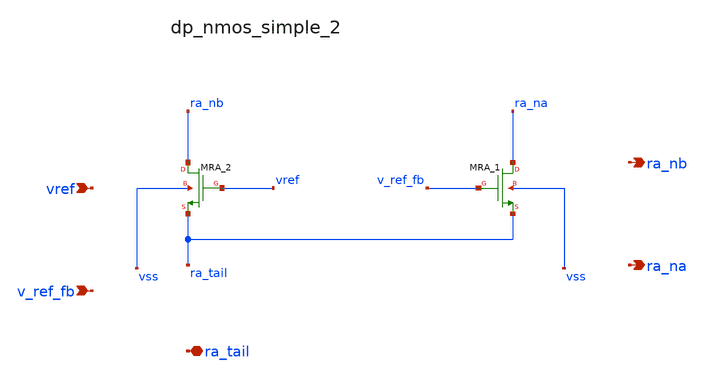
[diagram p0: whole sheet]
** sch_path: analog-db/raw/ldo_005_buffered_ref/hier/blocks/dp_nmos_simple_2.sch
**.subckt dp_nmos_simple_2 vref v_ref_fb ra_tail ra_nb ra_na
*.ipin vref
*.ipin v_ref_fb
*.iopin ra_tail
*.opin ra_nb
*.opin ra_na
XMRA_1 ra_na v_ref_fb ra_tail vss sg13_hv_nmos w=x_dut_xmra_1_w l=x_dut_xmra_1_l ng=1 m=1
XMRA_2 ra_nb vref ra_tail vss sg13_hv_nmos w=x_dut_xmra_2_w l=x_dut_xmra_2_l ng=1 m=1
**.ends
.end
